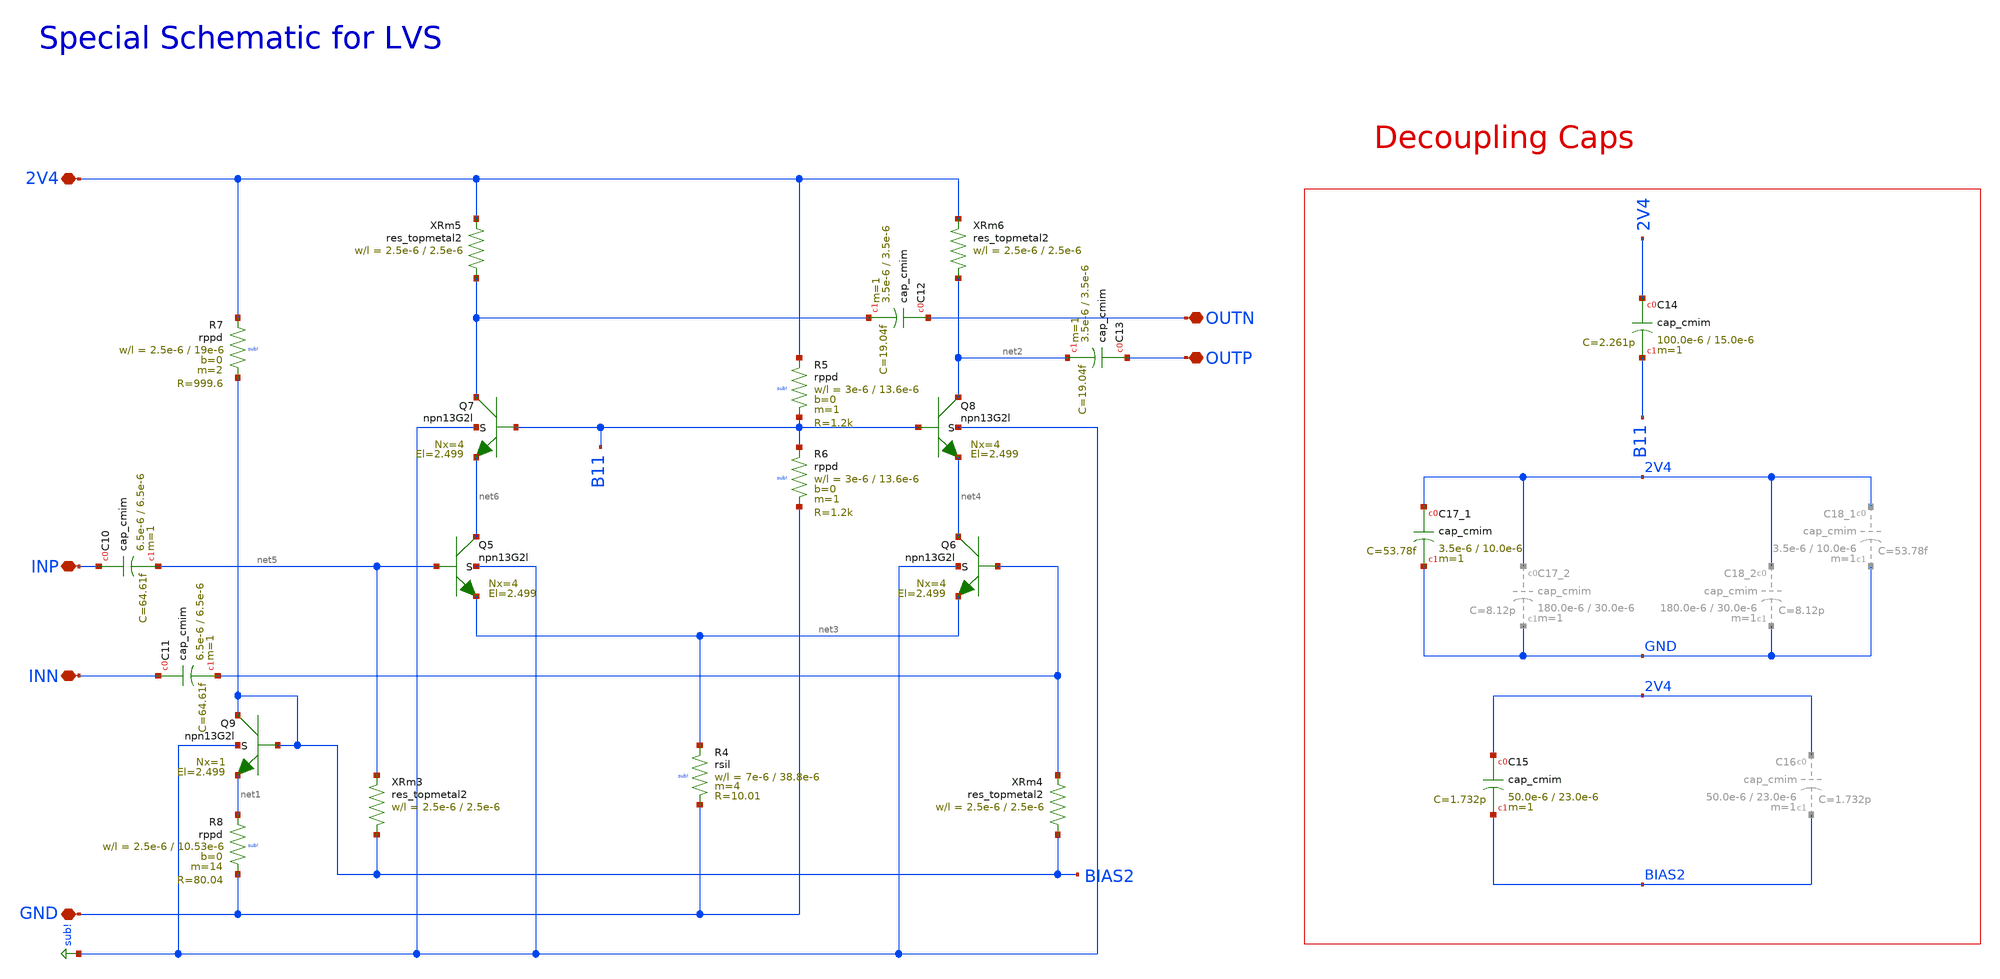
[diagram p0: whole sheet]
** sch_path: mWATTBAT/design_data/lvs/RFAMP_50GD_LVS.sch
**.subckt RFAMP_50GD_LVS 2V4 GND OUTN OUTP INP INN
*.iopin 2V4
*.iopin GND
*.iopin OUTN
*.iopin OUTP
*.iopin INP
*.iopin INN
XQ5 net6 net5 net3 sub! npn13G2l Nx=4 El=2.499 mm_ok=1
XQ6 net4 INN net3 sub! npn13G2l Nx=4 El=2.499 mm_ok=1
XQ9 BIAS2 BIAS2 net1 sub! npn13G2l Nx=1 El=2.499 mm_ok=1
XQ7 OUTN B11 net6 sub! npn13G2l Nx=4 El=2.499 mm_ok=1
XQ8 net2 B11 net4 sub! npn13G2l Nx=4 El=2.499 mm_ok=1
XR7 2V4 BIAS2 sub! rppd w=2.5e-6 l=19e-6 m=2 b=0 mm_ok=1
XC10 INP net5 cap_cmim w=6.5e-6 l=6.5e-6 m=1 mm_ok=1
XC13 OUTP net2 cap_cmim w=3.5e-6 l=3.5e-6 m=1 mm_ok=1
XC14 2V4 B11 cap_cmim w=100.0e-6 l=15.0e-6 m=1 mm_ok=1
XC15 2V4 BIAS2 cap_cmim w=50.0e-6 l=23.0e-6 m=1 mm_ok=1
XC17_1 2V4 GND cap_cmim w=3.5e-6 l=10.0e-6 m=1 mm_ok=1
XR6 B11 GND sub! rppd w=3e-6 l=13.6e-6 m=1 b=0 mm_ok=1
XR5 2V4 B11 sub! rppd w=3e-6 l=13.6e-6 m=1 b=0 mm_ok=1
XR8 net1 GND sub! rppd w=2.5e-6 l=10.53e-6 m=14 b=0 mm_ok=1
XR4 net3 GND sub! rsil w=7e-6 l=38.8e-6 m=4 mm_ok=1
XRm3 BIAS2 net5 res_topmetal2 w=2.5e-6 l=2.5e-6
XRm4 BIAS2 INN res_topmetal2 w=2.5e-6 l=2.5e-6
XRm5 OUTN 2V4 res_topmetal2 w=2.5e-6 l=2.5e-6
XRm6 net2 2V4 res_topmetal2 w=2.5e-6 l=2.5e-6
**.ends
.GLOBAL sub!
.end
